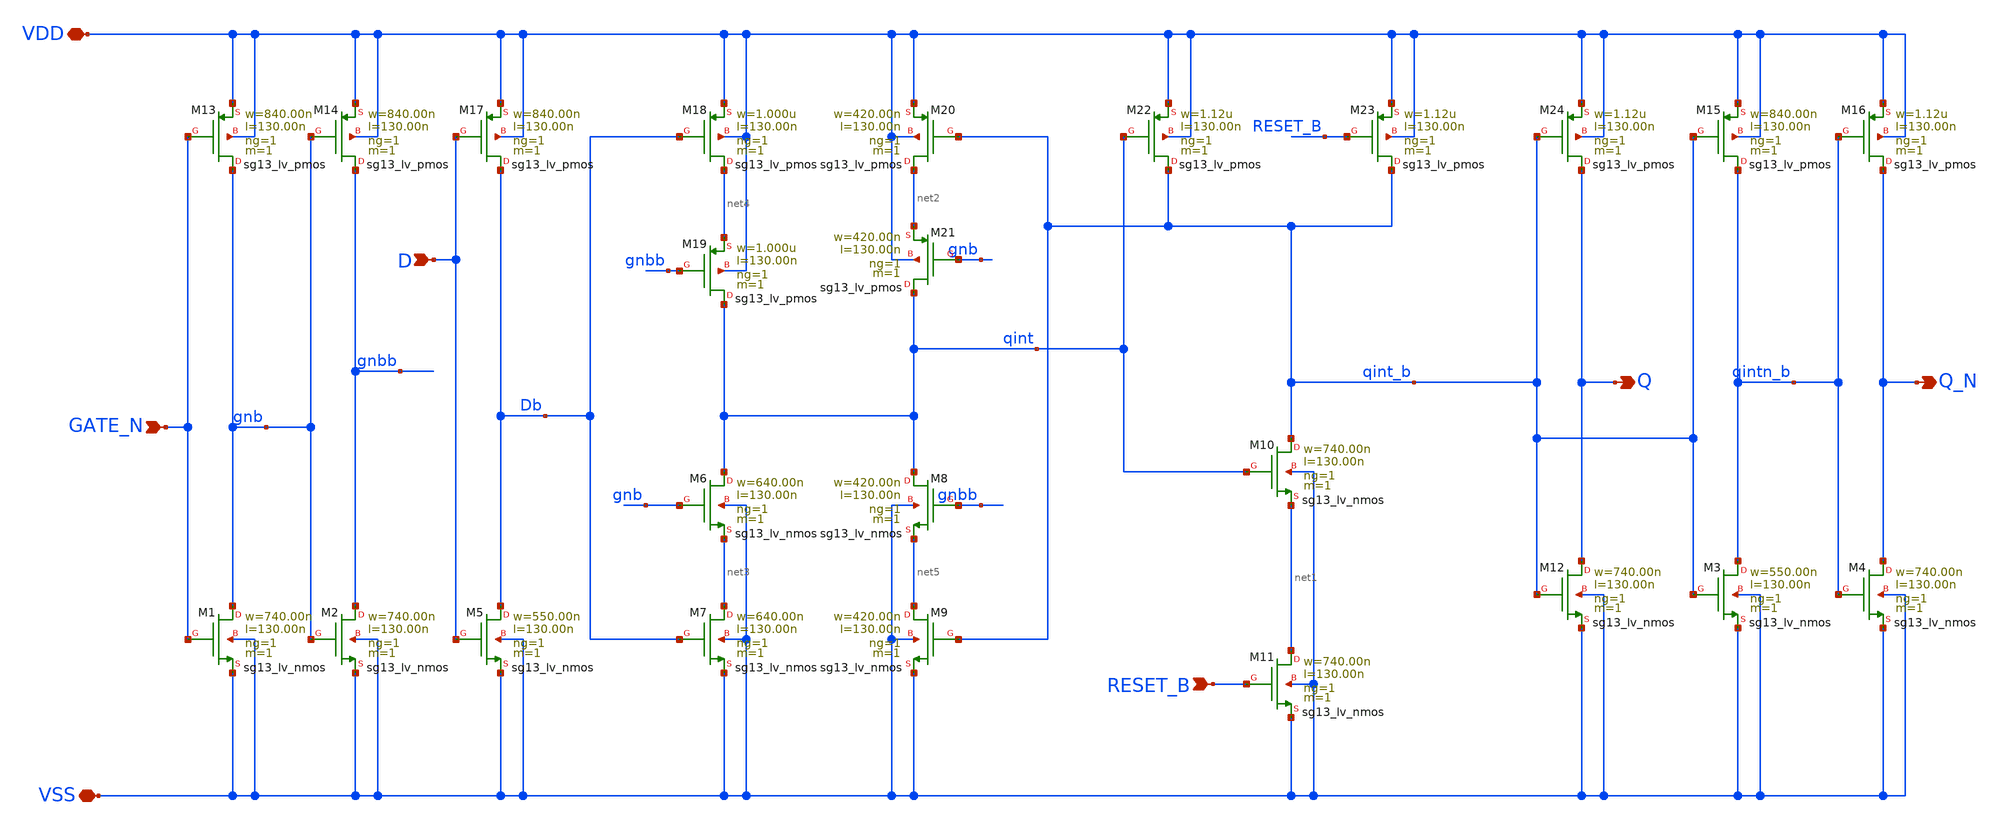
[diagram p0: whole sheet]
** sch_path: ihp-sg13g2/libs.tech/xschem/sg13g2_stdcells/sg13g2_dllr_1.sch
* Copyright 2023 IHP PDK Authors
* Licensed under the Apache License, Version 2.0 (the "License");
* you may not use this file except in compliance with the License.
* You may obtain a copy of the License at
* https://www.apache.org/licenses/LICENSE-2.0
* Unless required by applicable law or agreed to in writing, software
* distributed under the License is distributed on an "AS IS" BASIS,
* WITHOUT WARRANTIES OR CONDITIONS OF ANY KIND, either express or implied.
* See the License for the specific language governing permissions and
* limitations under the License.
**.subckt sg13g2_dllr_1 D GATE_N RESET_B Q Q_N VDD VSS
*.ipin D
*.ipin GATE_N
*.ipin RESET_B
*.opin Q
*.opin Q_N
*.iopin VDD
*.iopin VSS
XM1 gnb GATE_N VSS VSS sg13_lv_nmos w=740.00n l=130.00n ng=1 m=1 mm_ok=1
XM2 gnbb gnb VSS VSS sg13_lv_nmos w=740.00n l=130.00n ng=1 m=1 mm_ok=1
XM3 qintn_b qint_b VSS VSS sg13_lv_nmos w=550.00n l=130.00n ng=1 m=1 mm_ok=1
XM4 Q_N qintn_b VSS VSS sg13_lv_nmos w=740.00n l=130.00n ng=1 m=1 mm_ok=1
XM5 Db D VSS VSS sg13_lv_nmos w=550.00n l=130.00n ng=1 m=1 mm_ok=1
XM6 qint gnb net3 VSS sg13_lv_nmos w=640.00n l=130.00n ng=1 m=1 mm_ok=1
XM7 net3 Db VSS VSS sg13_lv_nmos w=640.00n l=130.00n ng=1 m=1 mm_ok=1
XM8 qint gnbb net5 VSS sg13_lv_nmos w=420.00n l=130.00n ng=1 m=1 mm_ok=1
XM9 net5 qint_b VSS VSS sg13_lv_nmos w=420.00n l=130.00n ng=1 m=1 mm_ok=1
XM10 qint_b qint net1 VSS sg13_lv_nmos w=740.00n l=130.00n ng=1 m=1 mm_ok=1
XM11 net1 RESET_B VSS VSS sg13_lv_nmos w=740.00n l=130.00n ng=1 m=1 mm_ok=1
XM12 Q qint_b VSS VSS sg13_lv_nmos w=740.00n l=130.00n ng=1 m=1 mm_ok=1
XM13 gnb GATE_N VDD VDD sg13_lv_pmos w=840.00n l=130.00n ng=1 m=1 mm_ok=1
XM14 gnbb gnb VDD VDD sg13_lv_pmos w=840.00n l=130.00n ng=1 m=1 mm_ok=1
XM15 qintn_b qint_b VDD VDD sg13_lv_pmos w=840.00n l=130.00n ng=1 m=1 mm_ok=1
XM16 Q_N qintn_b VDD VDD sg13_lv_pmos w=1.12u l=130.00n ng=1 m=1 mm_ok=1
XM17 Db D VDD VDD sg13_lv_pmos w=840.00n l=130.00n ng=1 m=1 mm_ok=1
XM18 net4 Db VDD VDD sg13_lv_pmos w=1.000u l=130.00n ng=1 m=1 mm_ok=1
XM19 qint gnbb net4 VDD sg13_lv_pmos w=1.000u l=130.00n ng=1 m=1 mm_ok=1
XM20 net2 qint_b VDD VDD sg13_lv_pmos w=420.00n l=130.00n ng=1 m=1 mm_ok=1
XM21 qint gnb net2 VDD sg13_lv_pmos w=420.00n l=130.00n ng=1 m=1 mm_ok=1
XM22 qint_b qint VDD VDD sg13_lv_pmos w=1.12u l=130.00n ng=1 m=1 mm_ok=1
XM23 qint_b RESET_B VDD VDD sg13_lv_pmos w=1.12u l=130.00n ng=1 m=1 mm_ok=1
XM24 Q qint_b VDD VDD sg13_lv_pmos w=1.12u l=130.00n ng=1 m=1 mm_ok=1
**.ends
.end
